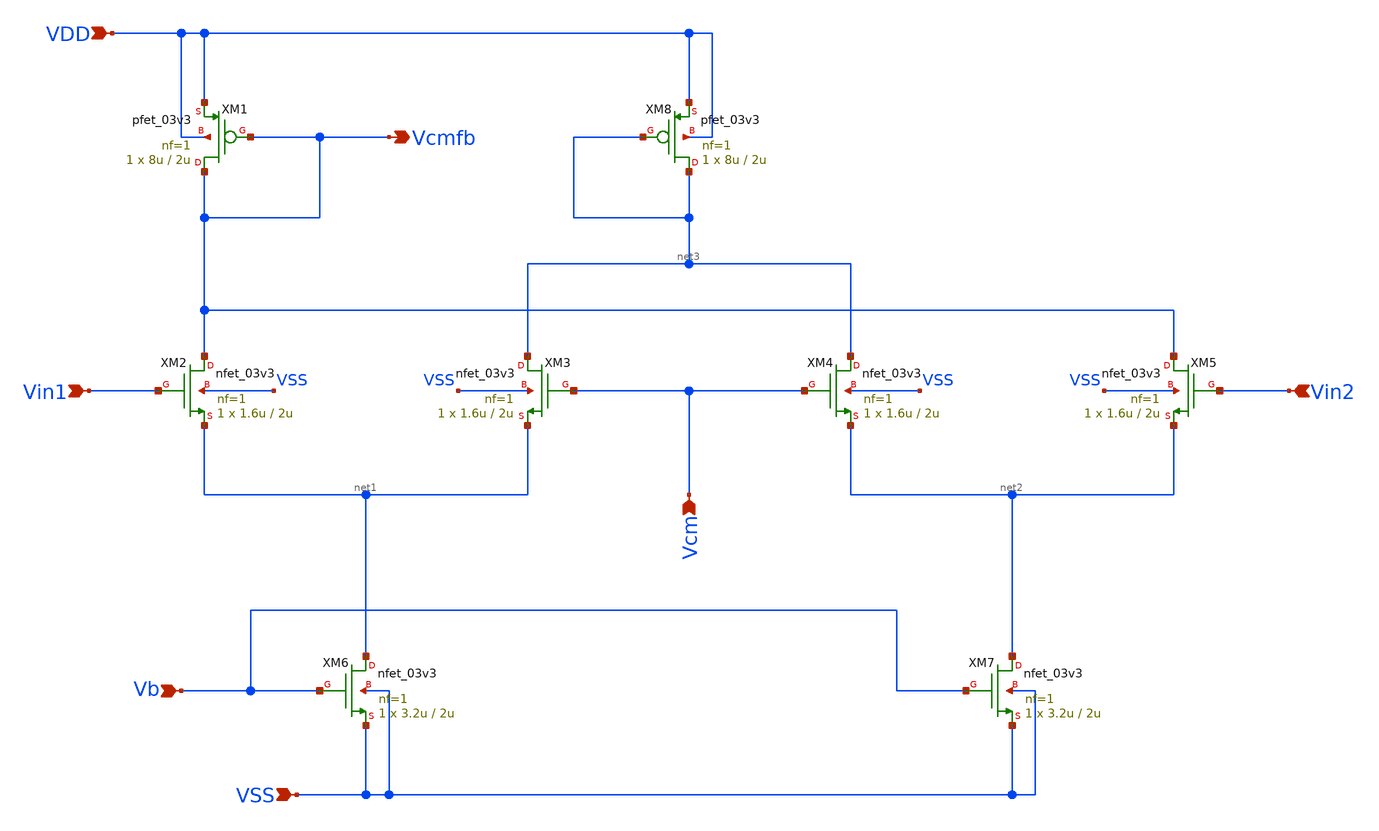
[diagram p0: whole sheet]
** sch_path: designs/libs/core_ina/ina_cmfb/ina_cmfb.sch
**.subckt ina_cmfb Vin1 Vin2 Vcmfb Vcm VSS Vb VDD
*.ipin Vin1
*.ipin Vin2
*.opin Vcmfb
*.ipin Vcm
*.ipin VSS
*.ipin Vb
*.ipin VDD
XM1 Vcmfb Vcmfb VDD VDD pfet_03v3 L=2u W=8u nf=1 ad='int((nf+1)/2) * W/nf * 0.18u' as='int((nf+2)/2) * W/nf * 0.18u'
+ pd='2*int((nf+1)/2) * (W/nf + 0.18u)' ps='2*int((nf+2)/2) * (W/nf + 0.18u)' nrd='0.18u / W' nrs='0.18u / W'
+ sa=0 sb=0 sd=0 m=1
XM2 Vcmfb Vin1 net1 VSS nfet_03v3 L=2u W=1.6u nf=1 ad='int((nf+1)/2) * W/nf * 0.18u' as='int((nf+2)/2) * W/nf * 0.18u'
+ pd='2*int((nf+1)/2) * (W/nf + 0.18u)' ps='2*int((nf+2)/2) * (W/nf + 0.18u)' nrd='0.18u / W' nrs='0.18u / W'
+ sa=0 sb=0 sd=0 m=1
XM3 net3 Vcm net1 VSS nfet_03v3 L=2u W=1.6u nf=1 ad='int((nf+1)/2) * W/nf * 0.18u' as='int((nf+2)/2) * W/nf * 0.18u'
+ pd='2*int((nf+1)/2) * (W/nf + 0.18u)' ps='2*int((nf+2)/2) * (W/nf + 0.18u)' nrd='0.18u / W' nrs='0.18u / W'
+ sa=0 sb=0 sd=0 m=1
XM6 net1 Vb VSS VSS nfet_03v3 L=2u W=3.2u nf=1 ad='int((nf+1)/2) * W/nf * 0.18u' as='int((nf+2)/2) * W/nf * 0.18u'
+ pd='2*int((nf+1)/2) * (W/nf + 0.18u)' ps='2*int((nf+2)/2) * (W/nf + 0.18u)' nrd='0.18u / W' nrs='0.18u / W'
+ sa=0 sb=0 sd=0 m=1
XM4 net3 Vcm net2 VSS nfet_03v3 L=2u W=1.6u nf=1 ad='int((nf+1)/2) * W/nf * 0.18u' as='int((nf+2)/2) * W/nf * 0.18u'
+ pd='2*int((nf+1)/2) * (W/nf + 0.18u)' ps='2*int((nf+2)/2) * (W/nf + 0.18u)' nrd='0.18u / W' nrs='0.18u / W'
+ sa=0 sb=0 sd=0 m=1
XM5 Vcmfb Vin2 net2 VSS nfet_03v3 L=2u W=1.6u nf=1 ad='int((nf+1)/2) * W/nf * 0.18u' as='int((nf+2)/2) * W/nf * 0.18u'
+ pd='2*int((nf+1)/2) * (W/nf + 0.18u)' ps='2*int((nf+2)/2) * (W/nf + 0.18u)' nrd='0.18u / W' nrs='0.18u / W'
+ sa=0 sb=0 sd=0 m=1
XM7 net2 Vb VSS VSS nfet_03v3 L=2u W=3.2u nf=1 ad='int((nf+1)/2) * W/nf * 0.18u' as='int((nf+2)/2) * W/nf * 0.18u'
+ pd='2*int((nf+1)/2) * (W/nf + 0.18u)' ps='2*int((nf+2)/2) * (W/nf + 0.18u)' nrd='0.18u / W' nrs='0.18u / W'
+ sa=0 sb=0 sd=0 m=1
XM8 net3 net3 VDD VDD pfet_03v3 L=2u W=8u nf=1 ad='int((nf+1)/2) * W/nf * 0.18u' as='int((nf+2)/2) * W/nf * 0.18u'
+ pd='2*int((nf+1)/2) * (W/nf + 0.18u)' ps='2*int((nf+2)/2) * (W/nf + 0.18u)' nrd='0.18u / W' nrs='0.18u / W'
+ sa=0 sb=0 sd=0 m=1
**.ends
.end
